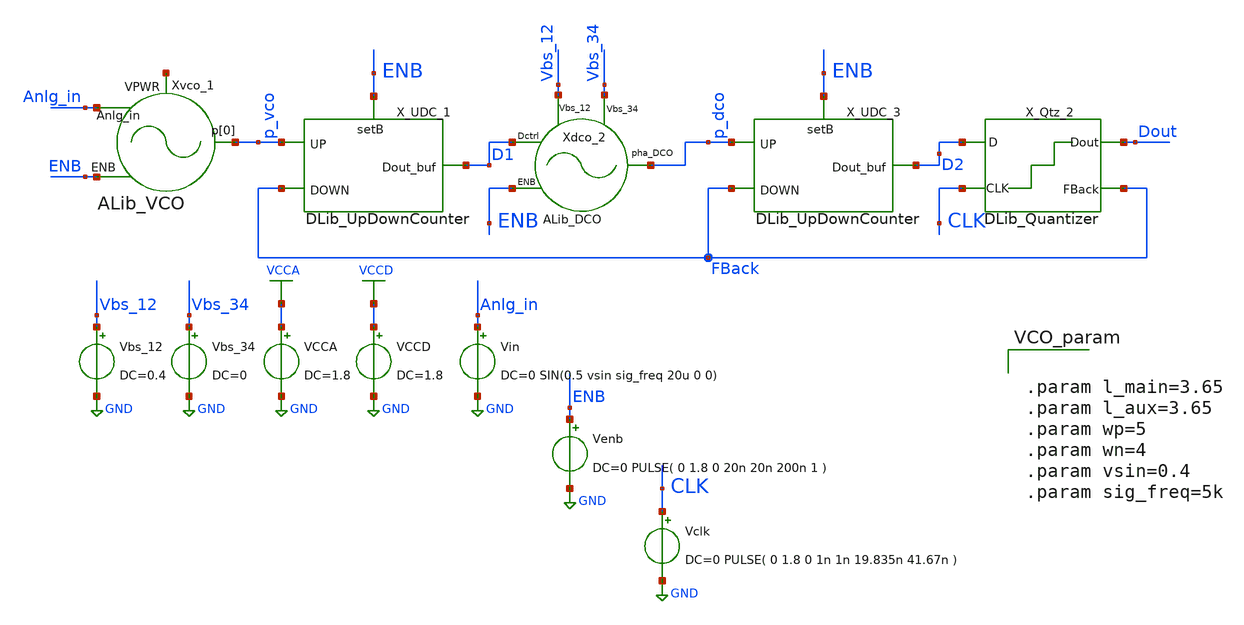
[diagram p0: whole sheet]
** sch_path: xschem/tb/vco_adc2_130nm_tb.sch

.include $::SKYWATER_STDCELLS/sky130_fd_sc_hd.spice
.lib $::SKYWATER_MODELS/sky130.lib.spice tt

**.subckt vco_adc2_130nm_tb
Vbs_34 Vbs_34 GND DC=0
VCCA VCCA GND DC=1.8
VCCD VCCD GND DC=1.8
Vin Anlg_in GND DC=0 SIN(0.5 vsin sig_freq 20u 0 0)
Venb ENB GND DC=0 PULSE( 0 1.8 0 20n 20n 200n 1 )
Vclk CLK GND DC=0 PULSE( 0 1.8 0 1n 1n 19.835n 41.67n )
Vbs_12 Vbs_12 GND DC=0.4
Xvco_1 net1 p_vco Anlg_in ENB ALib_VCO L12=0.15 Wp12=2.4 Wn12=1.2 L34=0.15 Wp34=1.2 Wn34=0.65
X_UDC_1 p_vco FBack ENB GND GND VCCD VCCD D1 DLib_UpDownCounter
Xdco_2 D1 ENB Vbs_12 Vbs_34 p_dco ALib_DCO
X_UDC_3 p_dco FBack ENB GND GND VCCD VCCD D2 DLib_UpDownCounter
X_Qtz_2 CLK D2 GND GND VCCD VCCD Dout FBack DLib_Quantizer
**** begin user architecture code


.param l_main=3.65
.param l_aux=3.65
.param wp=5
.param wn=4
.param vsin=0.4
.param sig_freq=5k

**** end user architecture code
**.ends
.GLOBAL GND
.GLOBAL VCCD
.GLOBAL VCCA
**** begin user architecture code


** control simulation lines
.probe tran v(p_vco) v(p_dco) v(xdco_1.p_osc) v(xdco_1.pha_ro) v(xdco_1.p_dco)  v(xdco_1.Isup) v(d1)
+ v(d2) v(dout) v(clk) v(fback) v(anlg_in) i(vcca) i(vccd)

.print v(clk) v(dout) v(anlg_in)

.tran 1n 0.5m start=0 $  sweep vin 0 1.0 0.1

.measure tran prd trig v(p_vco) val=0.8 rise=10 targ v(p_vco) val=0.8 rise=20
.measure tran freq_v param='10/prd'
.measure tran prd1 trig v(p_dco) val=0.8 rise=10 targ v(p_dco) val=0.8 rise=30
.measure tran freq_d param='20/prd1'
.measure tran I_analog avg i(vcca) from=0.1m to=1.1m
*.measure tran I_analog1 avg i(vcca1) from=0.1m to=1.1m
.measure tran I_digital avg i(vccd) from=0.1m to=1.1m
.measure tran A_power param='I_analog*1.8'
*.measure tran A_power1 param='I_analog1*1.8'
.measure tran D_power param='I_digital*1.8'
** options for finesim simulator
.option finesim_fsdb_version=5.6
.option finesim_output=fsdb
.option finesim_mode=spicead:p
.option finesim_mode=dlib*:promd:subckt
.option runlvl=7
*.option accurate=1
*.option finesim_mode=alib_vco:spicehd:subckt
*.option finesim_mode=prohd

** options for hspice simulator
*.option fsdb=1
*.option opfile=1 split_dp=1

**** end user architecture code


**** end user architecture code
.end
